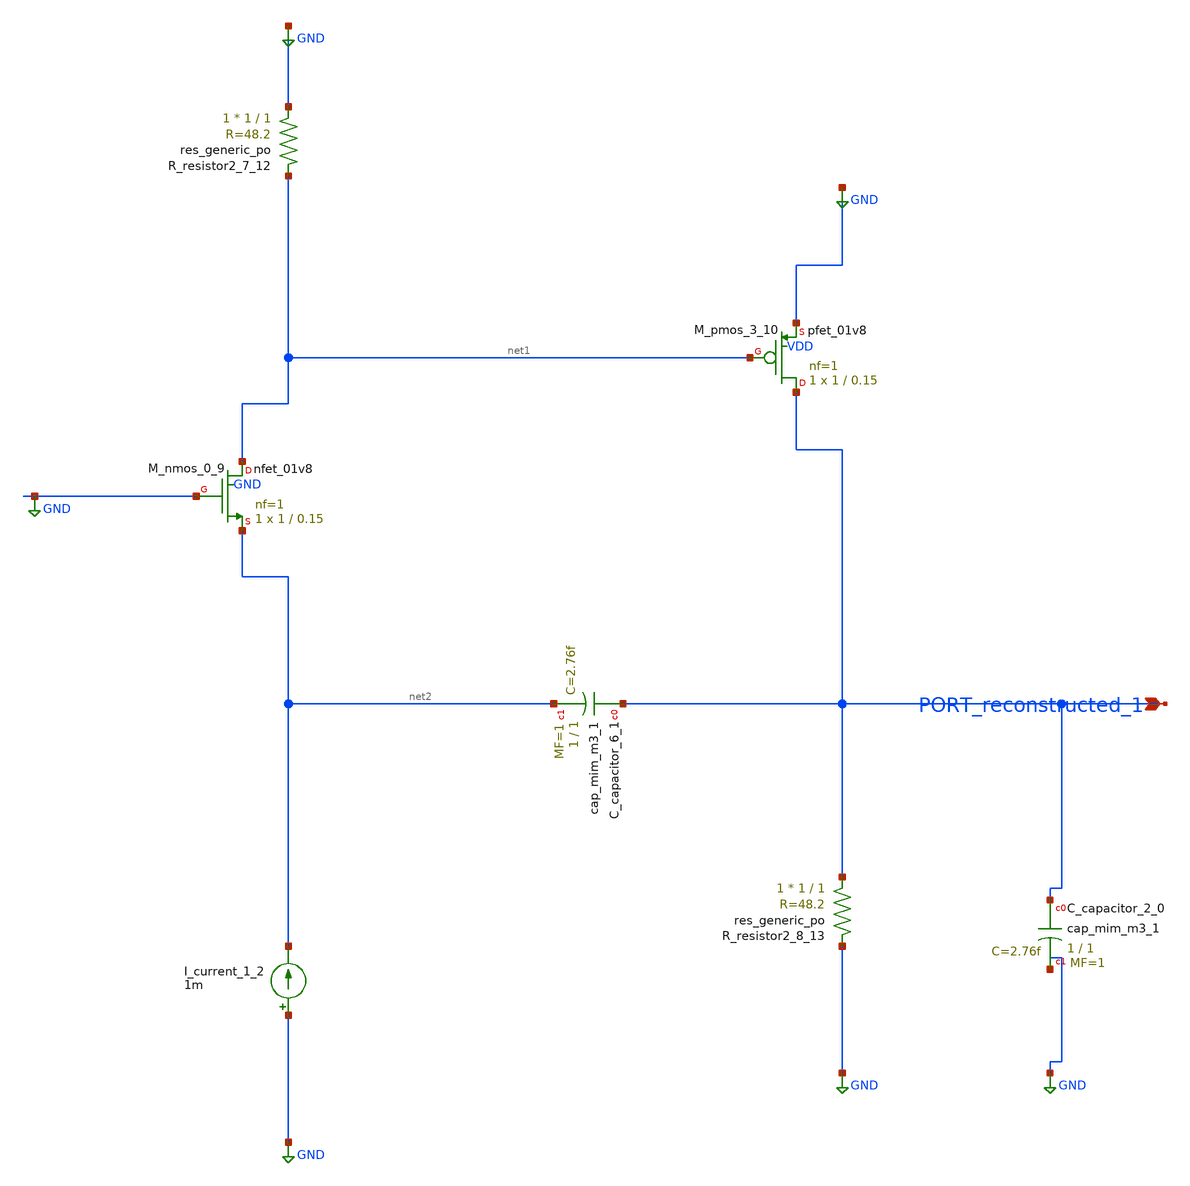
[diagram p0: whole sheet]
** sch_path: schematics/AMSNet/739.sch
**.subckt 739 PORT_reconstructed_1
*.ipin PORT_reconstructed_1
XC_capacitor_2_0 PORT_reconstructed_1 GND sky130_fd_pr__cap_mim_m3_1 W=1 L=1 MF=1 m=1
XC_capacitor_6_1 PORT_reconstructed_1 net2 sky130_fd_pr__cap_mim_m3_1 W=1 L=1 MF=1 m=1
I_current_1_2 GND net2 1m
XM_nmos_0_9 net1 GND net2 GND sky130_fd_pr__nfet_01v8 L=0.15 W=1 nf=1 ad='int((1 + 1)/2) * 1 / 1 * 0.29'
+ as='int((1 + 2)/2) * 1 / 1 * 0.29' pd='2*int((1 + 1)/2) * (1 / 1 + 0.29)' ps='2*int((1 + 2)/2) * (1 / 1 + 0.29)'
+ nrd='0.29 / 1 ' nrs='0.29 / 1 ' sa=0 sb=0 sd=0 mult=1 m=1
XM_pmos_3_10 PORT_reconstructed_1 net1 GND VDD sky130_fd_pr__pfet_01v8 L=0.15 W=1 nf=1 ad='int((1 + 1)/2) * 1 / 1 * 0.29'
+ as='int((1 + 2)/2) * 1 / 1 * 0.29' pd='2*int((1 + 1)/2) * (1 / 1 + 0.29)' ps='2*int((1 + 2)/2) * (1 / 1 + 0.29)'
+ nrd='0.29 / 1 ' nrs='0.29 / 1 ' sa=0 sb=0 sd=0 mult=1 m=1
XR_resistor2_7_12 GND net1 sky130_fd_pr__res_generic_po W=1 L=1 m=1
XR_resistor2_8_13 PORT_reconstructed_1 GND sky130_fd_pr__res_generic_po W=1 L=1 m=1
**.ends
.GLOBAL GND
.end
